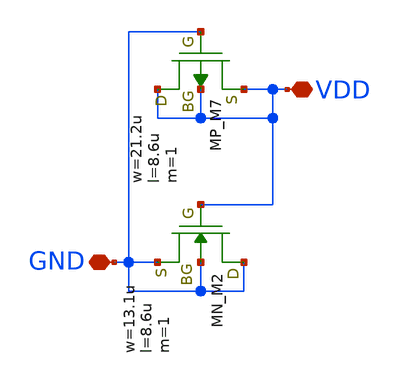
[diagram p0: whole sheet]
** sch_path: LEF/FILL3.sch
**.subckt FILL3 GND VDD
*.iopin GND
*.iopin VDD
XM7 VDD GND VDD VDD PMOS w=21.2u l=8.6u as=0 ad=0 ps=0 pd=0 nrd=0 nrs=0 m=1
XM2 GND VDD GND GND NMOS w=13.1u l=8.6u as=0 ad=0 ps=0 pd=0 nrd=0 nrs=0 m=1
**.ends
.end
